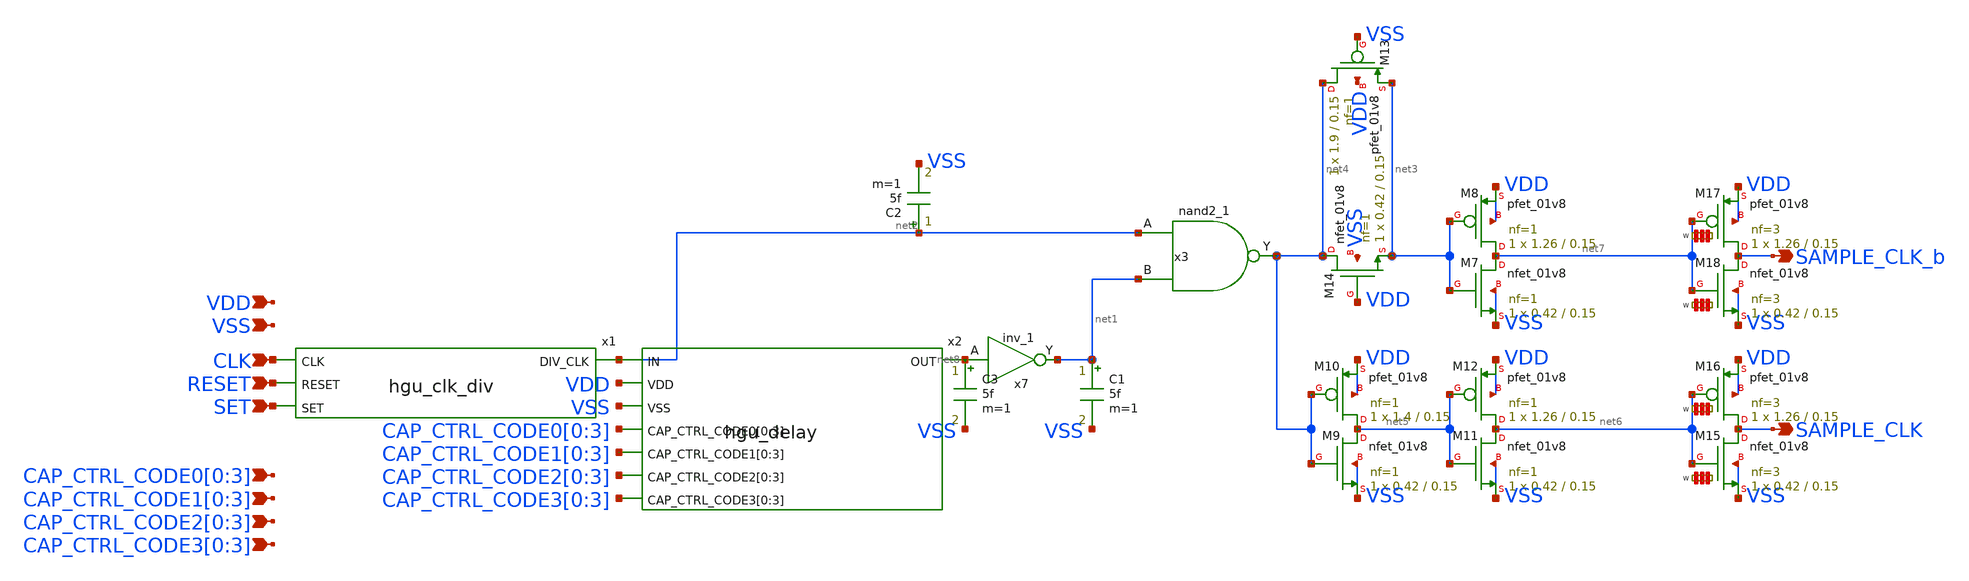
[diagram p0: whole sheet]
** sch_path: hgu/xschem/hgu_clk_sample.sch
**.subckt hgu_clk_sample VDD VSS SET RESET CLK SAMPLE_CLK SAMPLE_CLK_b
*+ CAP_CTRL_CODE1[0],CAP_CTRL_CODE1[1],CAP_CTRL_CODE1[2],CAP_CTRL_CODE1[3] CAP_CTRL_CODE2[0],CAP_CTRL_CODE2[1],CAP_CTRL_CODE2[2],CAP_CTRL_CODE2[3]
*+ CAP_CTRL_CODE3[0],CAP_CTRL_CODE3[1],CAP_CTRL_CODE3[2],CAP_CTRL_CODE3[3] CAP_CTRL_CODE0[0],CAP_CTRL_CODE0[1],CAP_CTRL_CODE0[2],CAP_CTRL_CODE0[3]
*.ipin VDD
*.ipin VSS
*.ipin SET
*.ipin RESET
*.ipin CLK
*.opin SAMPLE_CLK
*.opin SAMPLE_CLK_b
*.ipin CAP_CTRL_CODE1[0],CAP_CTRL_CODE1[1],CAP_CTRL_CODE1[2],CAP_CTRL_CODE1[3]
*.ipin CAP_CTRL_CODE2[0],CAP_CTRL_CODE2[1],CAP_CTRL_CODE2[2],CAP_CTRL_CODE2[3]
*.ipin CAP_CTRL_CODE3[0],CAP_CTRL_CODE3[1],CAP_CTRL_CODE3[2],CAP_CTRL_CODE3[3]
*.ipin CAP_CTRL_CODE0[0],CAP_CTRL_CODE0[1],CAP_CTRL_CODE0[2],CAP_CTRL_CODE0[3]
x1 net2 CLK RESET SET hgu_clk_div
x2 net8 net2 VDD VSS CAP_CTRL_CODE0[0] CAP_CTRL_CODE0[1] CAP_CTRL_CODE0[2] CAP_CTRL_CODE0[3]
+ CAP_CTRL_CODE1[0] CAP_CTRL_CODE1[1] CAP_CTRL_CODE1[2] CAP_CTRL_CODE1[3] CAP_CTRL_CODE2[0] CAP_CTRL_CODE2[1]
+ CAP_CTRL_CODE2[2] CAP_CTRL_CODE2[3] CAP_CTRL_CODE3[0] CAP_CTRL_CODE3[1] CAP_CTRL_CODE3[2] CAP_CTRL_CODE3[3] hgu_delay
+ DELAY_CAP=8f
x7 net8 VGND VNB VPB VPWR net1 sky130_fd_sc_hd__inv_1
C1 net1 VSS 5f m=1
C2 net2 VSS 5f m=1
C3 net8 VSS 5f m=1
x3 net2 net1 VGND VNB VPB VPWR net4 sky130_fd_sc_hd__nand2_1
XM7 net7 net3 VSS VSS sky130_fd_pr__nfet_01v8 L=0.15 W=0.42 nf=1 ad='int((nf+1)/2) * W/nf * 0.29' as='int((nf+2)/2) * W/nf * 0.29'
+ pd='2*int((nf+1)/2) * (W/nf + 0.29)' ps='2*int((nf+2)/2) * (W/nf + 0.29)' nrd='0.29 / W' nrs='0.29 / W'
+ sa=0 sb=0 sd=0 mult=1 m=1
XM8 net7 net3 VDD VDD sky130_fd_pr__pfet_01v8 L=0.15 W=1.26 nf=1 ad='int((nf+1)/2) * W/nf * 0.29' as='int((nf+2)/2) * W/nf * 0.29'
+ pd='2*int((nf+1)/2) * (W/nf + 0.29)' ps='2*int((nf+2)/2) * (W/nf + 0.29)' nrd='0.29 / W' nrs='0.29 / W'
+ sa=0 sb=0 sd=0 mult=1 m=1
XM9 net5 net4 VSS VSS sky130_fd_pr__nfet_01v8 L=0.15 W=0.42 nf=1 ad='int((nf+1)/2) * W/nf * 0.29' as='int((nf+2)/2) * W/nf * 0.29'
+ pd='2*int((nf+1)/2) * (W/nf + 0.29)' ps='2*int((nf+2)/2) * (W/nf + 0.29)' nrd='0.29 / W' nrs='0.29 / W'
+ sa=0 sb=0 sd=0 mult=1 m=1
XM10 net5 net4 VDD VDD sky130_fd_pr__pfet_01v8 L=0.15 W=1.4 nf=1 ad='int((nf+1)/2) * W/nf * 0.29' as='int((nf+2)/2) * W/nf * 0.29'
+ pd='2*int((nf+1)/2) * (W/nf + 0.29)' ps='2*int((nf+2)/2) * (W/nf + 0.29)' nrd='0.29 / W' nrs='0.29 / W'
+ sa=0 sb=0 sd=0 mult=1 m=1
XM11 net6 net5 VSS VSS sky130_fd_pr__nfet_01v8 L=0.15 W=0.42 nf=1 ad='int((nf+1)/2) * W/nf * 0.29' as='int((nf+2)/2) * W/nf * 0.29'
+ pd='2*int((nf+1)/2) * (W/nf + 0.29)' ps='2*int((nf+2)/2) * (W/nf + 0.29)' nrd='0.29 / W' nrs='0.29 / W'
+ sa=0 sb=0 sd=0 mult=1 m=1
XM12 net6 net5 VDD VDD sky130_fd_pr__pfet_01v8 L=0.15 W=1.26 nf=1 ad='int((nf+1)/2) * W/nf * 0.29' as='int((nf+2)/2) * W/nf * 0.29'
+ pd='2*int((nf+1)/2) * (W/nf + 0.29)' ps='2*int((nf+2)/2) * (W/nf + 0.29)' nrd='0.29 / W' nrs='0.29 / W'
+ sa=0 sb=0 sd=0 mult=1 m=1
XM13 net4 VSS net3 VDD sky130_fd_pr__pfet_01v8 L=0.15 W=1.9 nf=1 ad='int((nf+1)/2) * W/nf * 0.29' as='int((nf+2)/2) * W/nf * 0.29'
+ pd='2*int((nf+1)/2) * (W/nf + 0.29)' ps='2*int((nf+2)/2) * (W/nf + 0.29)' nrd='0.29 / W' nrs='0.29 / W'
+ sa=0 sb=0 sd=0 mult=1 m=1
XM14 net4 VDD net3 VSS sky130_fd_pr__nfet_01v8 L=0.15 W=0.42 nf=1 ad='int((nf+1)/2) * W/nf * 0.29' as='int((nf+2)/2) * W/nf * 0.29'
+ pd='2*int((nf+1)/2) * (W/nf + 0.29)' ps='2*int((nf+2)/2) * (W/nf + 0.29)' nrd='0.29 / W' nrs='0.29 / W'
+ sa=0 sb=0 sd=0 mult=1 m=1
XM15 SAMPLE_CLK net6 VSS VSS sky130_fd_pr__nfet_01v8 L=0.15 W='0.42 * 3 ' nf=3 ad='int((nf+1)/2) * W / nf * 0.29'
+ as='int((nf+2)/2) * W / nf * 0.29' pd='2*int((nf+1)/2) * (W / nf + 0.29)' ps='2*int((nf+2)/2) * (W / nf + 0.29)'
+ nrd='0.29 / W ' nrs='0.29 / W ' sa=0 sb=0 sd=0 mult=1 m=1
XM16 SAMPLE_CLK net6 VDD VDD sky130_fd_pr__pfet_01v8 L=0.15 W='1.26 * 3 ' nf=3 ad='int((nf+1)/2) * W / nf * 0.29'
+ as='int((nf+2)/2) * W / nf * 0.29' pd='2*int((nf+1)/2) * (W / nf + 0.29)' ps='2*int((nf+2)/2) * (W / nf + 0.29)'
+ nrd='0.29 / W ' nrs='0.29 / W ' sa=0 sb=0 sd=0 mult=1 m=1
XM17 SAMPLE_CLK_b net7 VDD VDD sky130_fd_pr__pfet_01v8 L=0.15 W='1.26 * 3 ' nf=3 ad='int((nf+1)/2) * W / nf * 0.29'
+ as='int((nf+2)/2) * W / nf * 0.29' pd='2*int((nf+1)/2) * (W / nf + 0.29)' ps='2*int((nf+2)/2) * (W / nf + 0.29)'
+ nrd='0.29 / W ' nrs='0.29 / W ' sa=0 sb=0 sd=0 mult=1 m=1
XM18 SAMPLE_CLK_b net7 VSS VSS sky130_fd_pr__nfet_01v8 L=0.15 W='0.42 * 3 ' nf=3 ad='int((nf+1)/2) * W / nf * 0.29'
+ as='int((nf+2)/2) * W / nf * 0.29' pd='2*int((nf+1)/2) * (W / nf + 0.29)' ps='2*int((nf+2)/2) * (W / nf + 0.29)'
+ nrd='0.29 / W ' nrs='0.29 / W ' sa=0 sb=0 sd=0 mult=1 m=1
**.ends
.end
